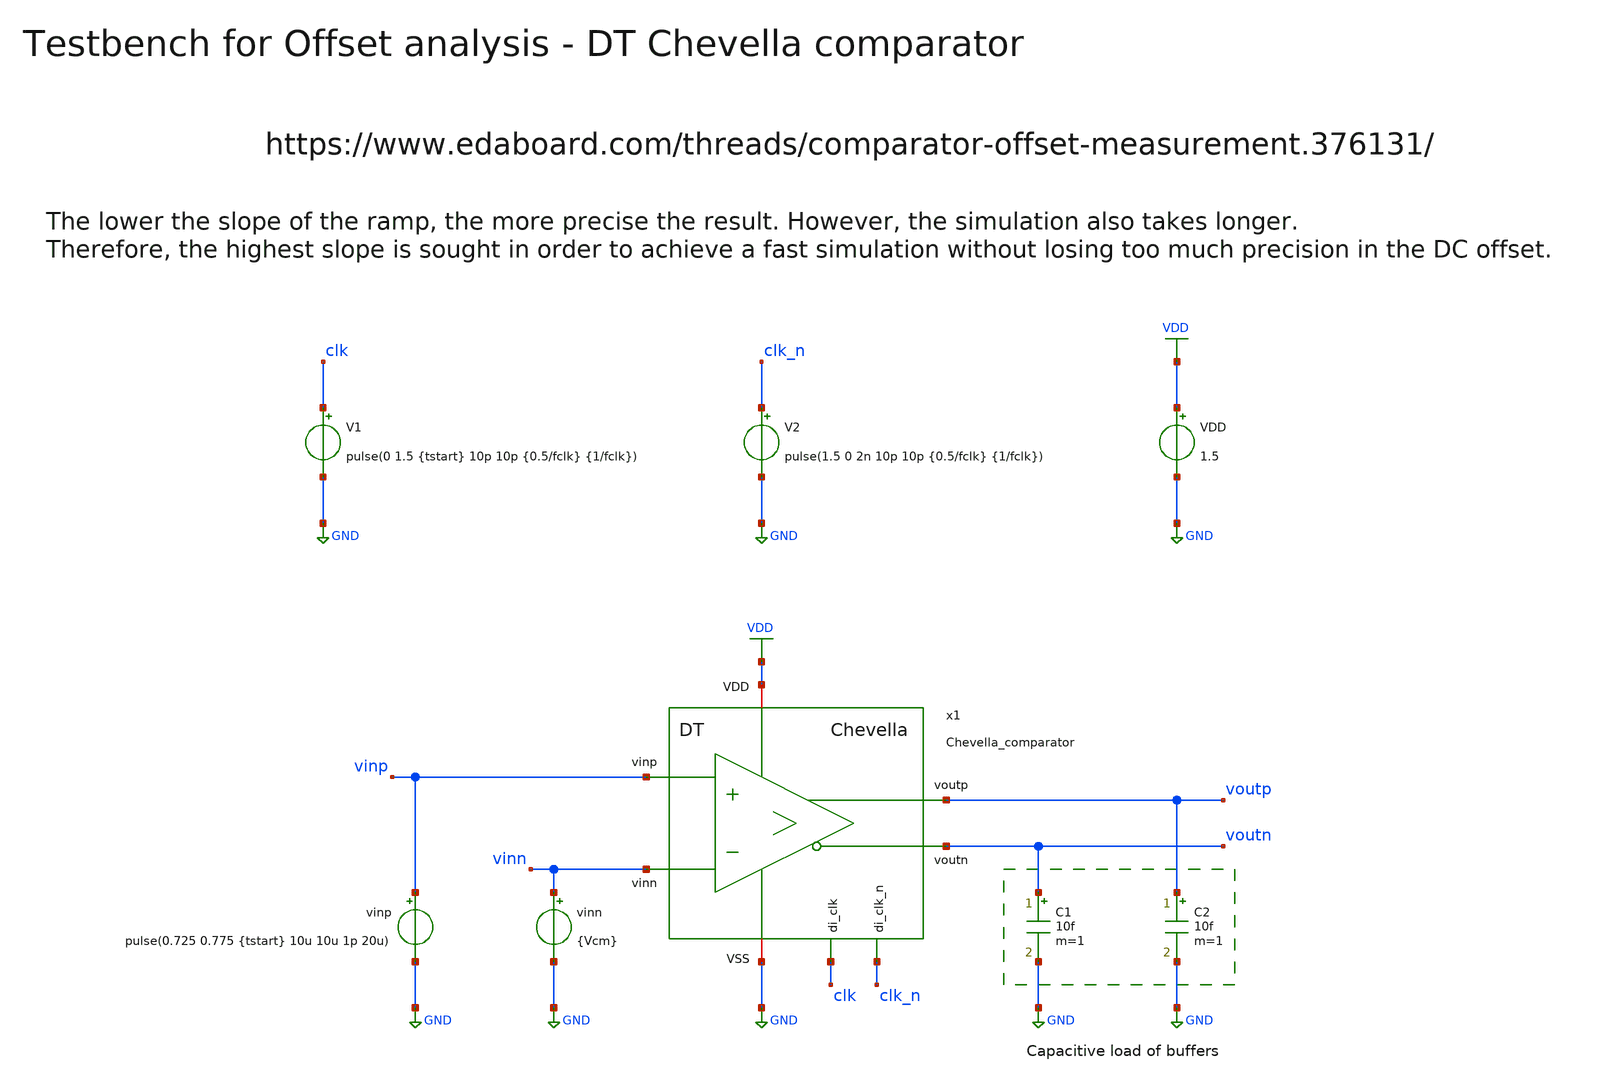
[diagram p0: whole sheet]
** sch_path: SG13G2_ATBS-ADC-main/xschem/comparator/discrete_time/Chevella/testbenches/Chevella_comparator_tb_tran_offset.sch
**.subckt Chevella_comparator_tb_tran_offset
VDD VDD GND 1.5
V1 clk GND pulse(0 1.5 {tstart} 10p 10p {0.5/fclk} {1/fclk})
vinn vinn GND {Vcm}
vinp vinp GND pulse(0.725 0.775 {tstart} 10u 10u 1p 20u)
V2 clk_n GND pulse(1.5 0 2n 10p 10p {0.5/fclk} {1/fclk})
C1 voutn GND 10f m=1
C2 voutp GND 10f m=1
x1 clk_n clk VDD voutp vinp GND voutn vinn Chevella_comparator
**** begin user architecture code

.lib cornerMOSlv.lib mos_tt
.lib cornerMOShv.lib mos_tt
.lib cornerRES.lib res_typ



.param temp=27
.param fclk=8000000
.param tstart=2n
.param Vcm=0.75
.csparam fclk=fclk
.csparam tstart=tstart
.csparam Vcm=Vcm
.options klu method=gear reltol=1e-3 abstol=1e-12 gmin=1e-15
.control
* save all

* User Constants
let tstop = 20u
let tstep = 1/fclk

* Operating Point Analysis
op
remzerovec
write Chevella_comparator_tb_tran_offset.raw
set appendwrite

* Transient Analysis
tran $&tstep $&tstop
write Chevella_comparator_tb_tran_offset.raw

* Measure offset increasing ramp
let voutp_limit = 0.9 * 1.5
meas tran tcross WHEN v(voutp)=voutp_limit RISE=1
print tcross
meas tran vinp_voff FIND v(vinp) at=tcross
let voff_inc = vinp_voff - Vcm
print voff_inc

* Measure offset decreasing ramp
let voutn_limit = 0.9 * 1.5
let tmiddle = tstop/2
meas tran tcross WHEN v(voutn)=voutn_limit from=tmiddle RISE=1
print tcross
meas tran vinp_voff FIND v(vinp) at=tcross
let voff_dec = vinp_voff - Vcm
print voff_dec

* Plotting
plot v(clk) v(voutp) v(voutn) v(vinp) v(vinn)

*quit
.endc

**** end user architecture code
**.ends

* expanding   symbol:  comparator/discrete_time/Chevella/Chevella_comparator.sym # of pins=8
** sym_path: SG13G2_ATBS-ADC-main/xschem/comparator/discrete_time/Chevella/Chevella_comparator.sym
** sch_path: SG13G2_ATBS-ADC-main/xschem/comparator/discrete_time/Chevella/Chevella_comparator.sch
.subckt Chevella_comparator di_clk_n di_clk VDD voutp vinp VSS voutn vinn
*.iopin VDD
*.opin voutp
*.opin voutn
*.ipin di_clk_n
*.iopin VSS
*.ipin vinp
*.ipin vinn
*.ipin di_clk
XM1a vcpn vinp net1 VSS sg13_lv_nmos w=1.0u l=0.13u ng=1 m=1 mm_ok=1
XM2a vcpp vinn net2 VSS sg13_lv_nmos w=1.0u l=0.13u ng=1 m=1 mm_ok=1
XM3 vs di_clk VSS VSS sg13_lv_nmos w=1.0u l=0.13u ng=1 m=1 mm_ok=1
XM4a vcpn di_clk VDD VDD sg13_lv_pmos w=1.0u l=0.13u ng=1 m=1 mm_ok=1
XM5a vcpp di_clk VDD VDD sg13_lv_pmos w=1.0u l=0.13u ng=1 m=1 mm_ok=1
XM12 voutp di_clk_n VSS VSS sg13_lv_nmos w=1.0u l=0.13u ng=1 m=1 mm_ok=1
XM8 net3 voutn VDD VDD sg13_lv_pmos w=2.0u l=0.13u ng=2 m=1 mm_ok=1
XM10 voutp voutn VSS VSS sg13_lv_nmos w=1.0u l=0.13u ng=1 m=1 mm_ok=1
XM11 voutn voutp VSS VSS sg13_lv_nmos w=1.0u l=0.13u ng=1 m=1 mm_ok=1
XM13 voutn di_clk_n VSS VSS sg13_lv_nmos w=1.0u l=0.13u ng=1 m=1 mm_ok=1
CP1 vcpn VSS 300f m=1
CP2 vcpp VSS 300f m=1
XM9 net4 voutp VDD VDD sg13_lv_pmos w=2.0u l=0.13u ng=2 m=1 mm_ok=1
XM6 voutp vcpn net3 VDD sg13_lv_pmos w=2.0u l=0.13u ng=2 m=1 mm_ok=1
XM7 voutn vcpp net4 VDD sg13_lv_pmos w=2.0u l=0.13u ng=2 m=1 mm_ok=1
XM4b net1 di_clk VDD VDD sg13_lv_pmos w=1.0u l=0.13u ng=1 m=1 mm_ok=1
XM5b net2 di_clk VDD VDD sg13_lv_pmos w=1.0u l=0.13u ng=1 m=1 mm_ok=1
XM1b net1 vcpp vs VSS sg13_lv_nmos w=1.0u l=0.13u ng=1 m=1 mm_ok=1
XM2b net2 vcpn vs VSS sg13_lv_nmos w=1.0u l=0.13u ng=1 m=1 mm_ok=1
.ends

.GLOBAL GND
.GLOBAL VDD
.end
